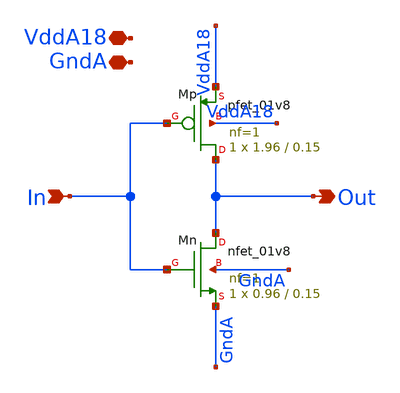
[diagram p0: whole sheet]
** sch_path: analog/klayout/production/final_merge_20260923/testbenches/cace/analog/xschem/Inverter1.sch
**.subckt Inverter1 In GndA VddA18 Out
*.ipin In
*.iopin GndA
*.iopin VddA18
*.opin Out
XMp Out In VddA18 VddA18 sky130_fd_pr__pfet_01v8 L=0.15 W=1.96 nf=1 ad='int((1 + 1)/2) * 1.96 / 1 * 0.29'
+ as='int((1 + 2)/2) * 1.96 / 1 * 0.29' pd='2*int((1 + 1)/2) * (1.96 / 1 + 0.29)' ps='2*int((1 + 2)/2) * (1.96 / 1 + 0.29)'
+ nrd='0.29 / 1.96 ' nrs='0.29 / 1.96 ' sa=0 sb=0 sd=0 mult=1 m=1
XMn Out In GndA GndA sky130_fd_pr__nfet_01v8 L=0.15 W=0.96 nf=1 ad='int((1 + 1)/2) * 0.96 / 1 * 0.29'
+ as='int((1 + 2)/2) * 0.96 / 1 * 0.29' pd='2*int((1 + 1)/2) * (0.96 / 1 + 0.29)' ps='2*int((1 + 2)/2) * (0.96 / 1 + 0.29)'
+ nrd='0.29 / 0.96 ' nrs='0.29 / 0.96 ' sa=0 sb=0 sd=0 mult=1 m=1
**.ends
.end
